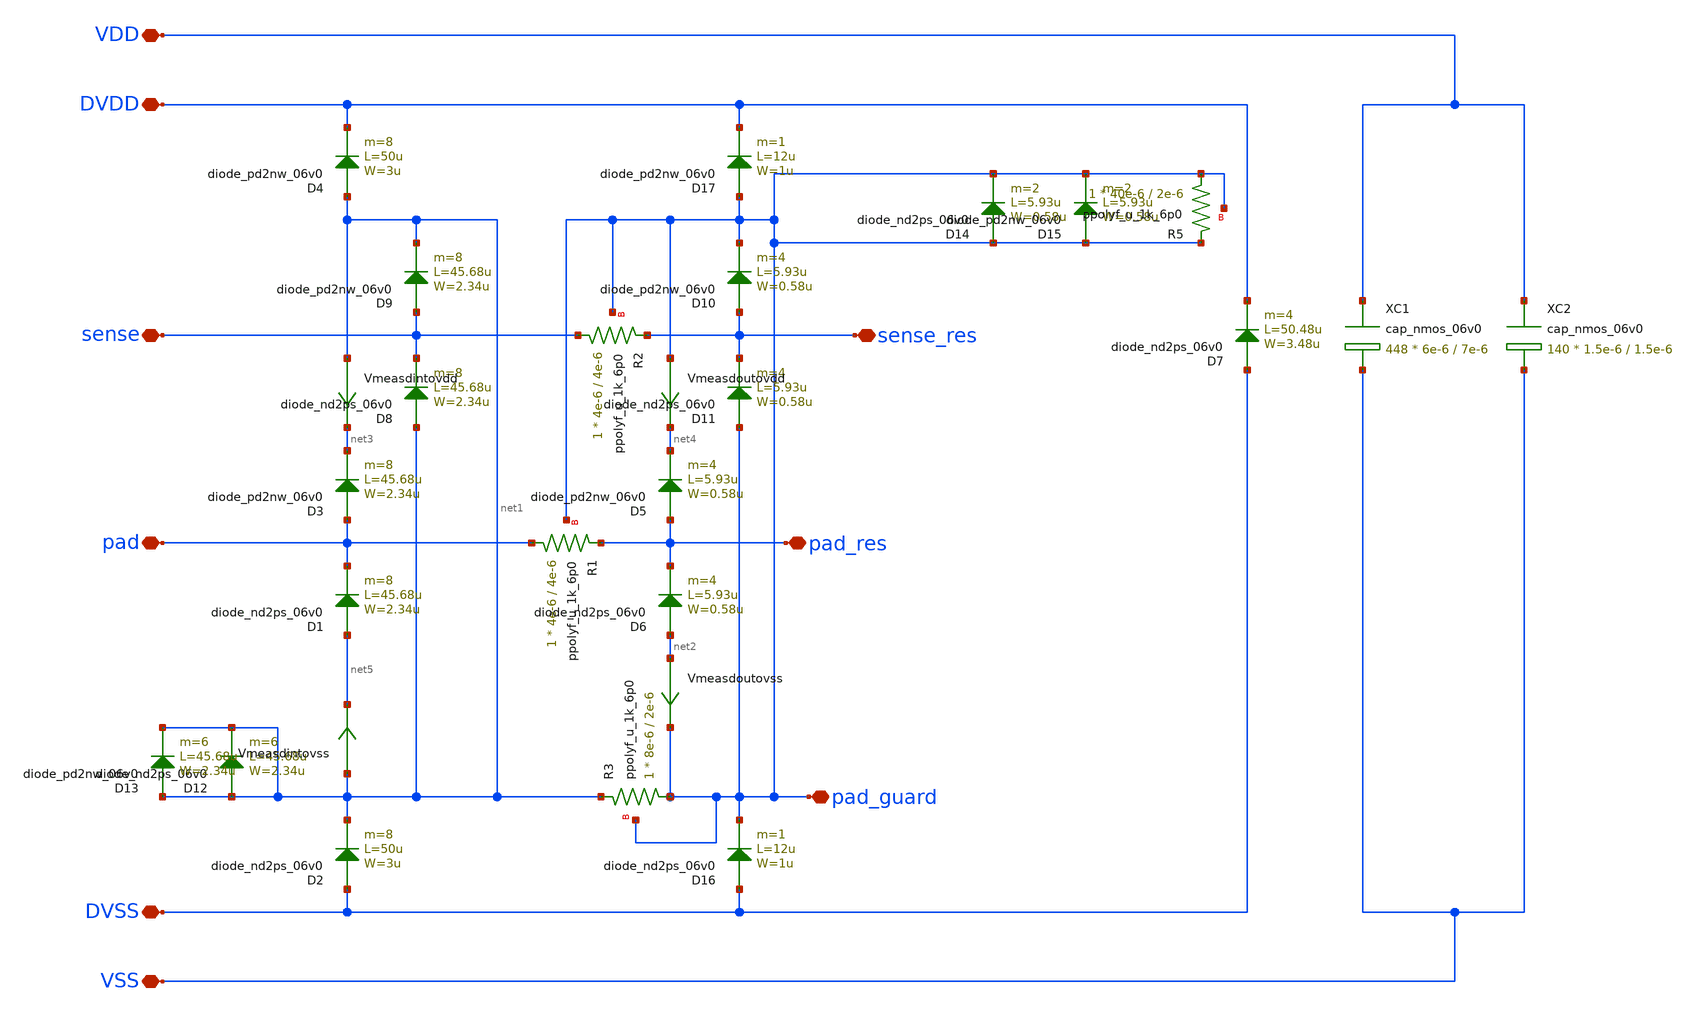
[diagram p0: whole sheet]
** sch_path: gf180mcuD/xschem-simul/gf180mcu_liplib__asig_guard_sense_5p0_dev.sch
**.subckt gf180mcu_liplib__asig_guard_sense_5p0_dev pad pad_guard DVDD DVSS pad_res sense sense_res
*+ VDD VSS
*.iopin pad
*.iopin pad_guard
*.iopin DVDD
*.iopin DVSS
*.iopin pad_res
*.iopin sense
*.iopin sense_res
*.iopin VDD
*.iopin VSS
D1 net5 pad diode_nd2ps_06v0 area='2.34u * 45.68u ' pj='2*2.34u + 2*45.68u ' m=8
D2 DVSS net1 diode_nd2ps_06v0 area='3u * 50u ' pj='2*3u + 2*50u ' m=8
D3 pad net3 diode_pd2nw_06v0 area='2.34u * 45.68u ' pj='2*2.34u + 2*45.68u ' m=8
D4 net1 DVDD diode_pd2nw_06v0 area='3u * 50u ' pj='2*3u + 2*50u ' m=8
XR1 pad pad_res pad_guard ppolyf_u_1k_6p0 r_width=4e-6 r_length=4e-6 m=1
D5 pad_res net4 diode_pd2nw_06v0 area='0.58u * 5.93u ' pj='2*0.58u + 2*5.93u ' m=4
D6 net2 pad_res diode_nd2ps_06v0 area='0.58u * 5.93u ' pj='2*0.58u + 2*5.93u ' m=4
D7 DVSS DVDD diode_nd2ps_06v0 area='3.48u * 50.48u ' pj='2*3.48u + 2*50.48u ' m=4
D8 net1 sense diode_nd2ps_06v0 area='2.34u * 45.68u ' pj='2*2.34u + 2*45.68u ' m=8
D9 sense net1 diode_pd2nw_06v0 area='2.34u * 45.68u ' pj='2*2.34u + 2*45.68u ' m=8
XR2 sense sense_res pad_guard ppolyf_u_1k_6p0 r_width=4e-6 r_length=4e-6 m=1
D10 sense_res pad_guard diode_pd2nw_06v0 area='0.58u * 5.93u ' pj='2*0.58u + 2*5.93u ' m=4
D11 pad_guard sense_res diode_nd2ps_06v0 area='0.58u * 5.93u ' pj='2*0.58u + 2*5.93u ' m=4
D14 pad_guard pad_guard diode_nd2ps_06v0 area='0.58u * 5.93u ' pj='2*0.58u + 2*5.93u ' m=2
D15 pad_guard pad_guard diode_pd2nw_06v0 area='0.58u * 5.93u ' pj='2*0.58u + 2*5.93u ' m=2
D12 net1 net1 diode_nd2ps_06v0 area='2.34u * 45.68u ' pj='2*2.34u + 2*45.68u ' m=6
D13 net1 net1 diode_pd2nw_06v0 area='2.34u * 45.68u ' pj='2*2.34u + 2*45.68u ' m=6
XR5 pad_guard pad_guard pad_guard ppolyf_u_1k_6p0 r_width=40e-6 r_length=2e-6 m=1
XC1 VDD VSS cap_nmos_06v0 c_width=6e-6 c_length=7e-6 m=448
XC2 VDD VSS cap_nmos_06v0 c_width=1.5e-6 c_length=1.5e-6 m=140
XR3 pad_guard net1 pad_guard ppolyf_u_1k_6p0 r_width=8e-6 r_length=2e-6 m=1
D16 DVSS pad_guard diode_nd2ps_06v0 area='1u * 12u ' pj='2*1u + 2*12u ' m=1
D17 pad_guard DVDD diode_pd2nw_06v0 area='1u * 12u ' pj='2*1u + 2*12u ' m=1
Vmeasdintovss net1 net5 0
.save i(vmeasdintovss)
Vmeasdintovdd net1 net3 0
.save i(vmeasdintovdd)
Vmeasdoutovdd pad_guard net4 0
.save i(vmeasdoutovdd)
Vmeasdoutovss net2 pad_guard 0
.save i(vmeasdoutovss)
**.ends
.end
